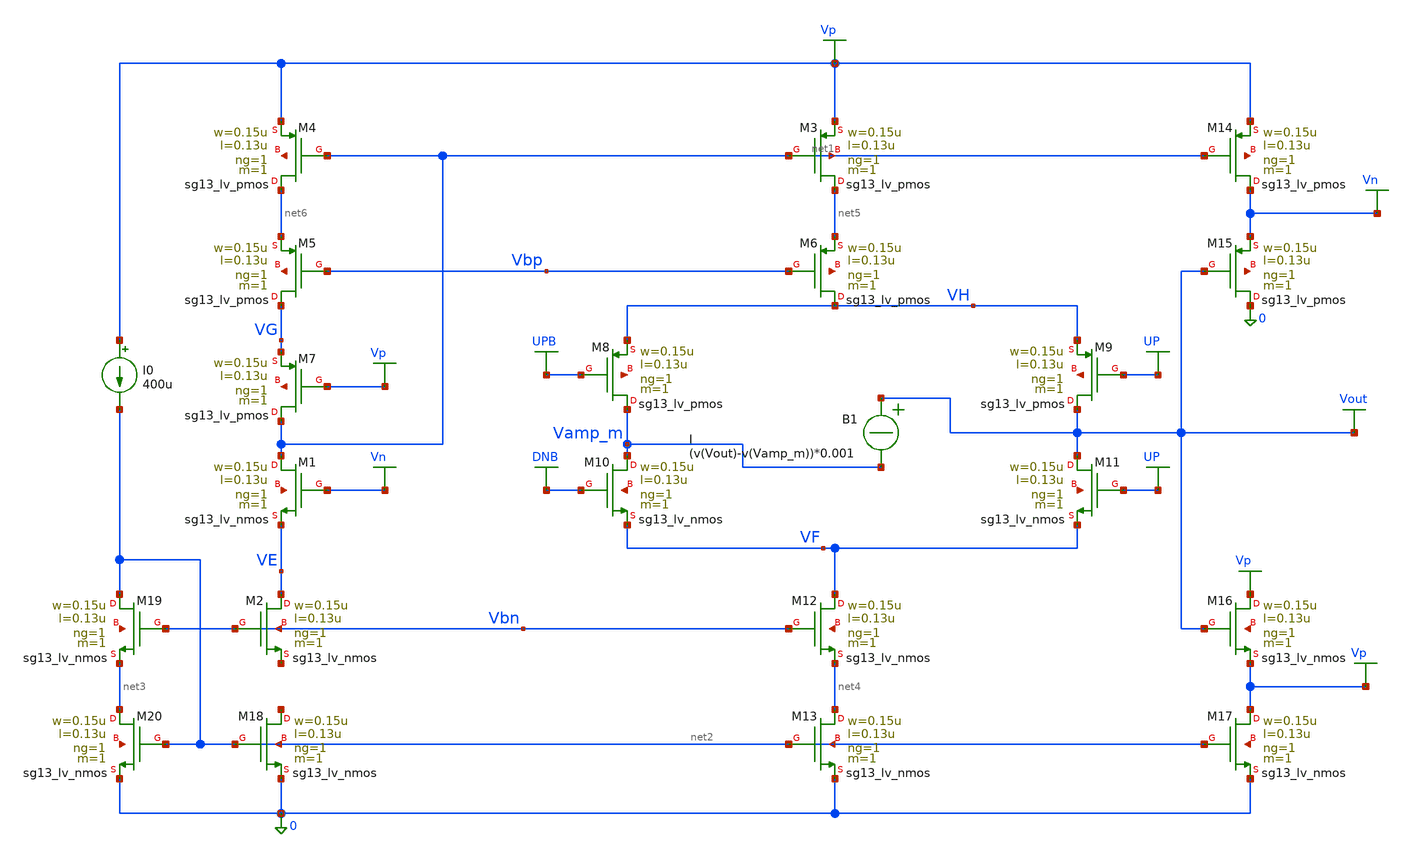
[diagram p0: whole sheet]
** sch_path: charge_pump/cp_v1.sch
**.subckt cp_v1
XM1 net1 Vn VE net7 sg13_lv_nmos w=0.15u l=0.13u ng=1 m=1 mm_ok=1
XM3 net5 net1 Vp net1 sg13_lv_pmos w=0.15u l=0.13u ng=1 m=1 mm_ok=1
XM4 net6 net1 Vp net8 sg13_lv_pmos w=0.15u l=0.13u ng=1 m=1 mm_ok=1
XM5 VG Vbp net6 net9 sg13_lv_pmos w=0.15u l=0.13u ng=1 m=1 mm_ok=1
XM6 VH Vbp net5 net10 sg13_lv_pmos w=0.15u l=0.13u ng=1 m=1 mm_ok=1
XM7 net1 Vp VG net11 sg13_lv_pmos w=0.15u l=0.13u ng=1 m=1 mm_ok=1
XM8 Vamp_m UPB VH net12 sg13_lv_pmos w=0.15u l=0.13u ng=1 m=1 mm_ok=1
XM9 Vout UP VH net13 sg13_lv_pmos w=0.15u l=0.13u ng=1 m=1 mm_ok=1
XM10 Vamp_m DNB VF net14 sg13_lv_nmos w=0.15u l=0.13u ng=1 m=1 mm_ok=1
XM11 Vout UP VF net15 sg13_lv_nmos w=0.15u l=0.13u ng=1 m=1 mm_ok=1
XM12 VF Vbn net4 net16 sg13_lv_nmos w=0.15u l=0.13u ng=1 m=1 mm_ok=1
XM13 net4 net2 0 net2 sg13_lv_nmos w=0.15u l=0.13u ng=1 m=1 mm_ok=1
XM14 Vn net1 Vp net17 sg13_lv_pmos w=0.15u l=0.13u ng=1 m=1 mm_ok=1
XM15 0 Vout Vn net18 sg13_lv_pmos w=0.15u l=0.13u ng=1 m=1 mm_ok=1
XM16 Vp Vout Vp net19 sg13_lv_nmos w=0.15u l=0.13u ng=1 m=1 mm_ok=1
XM17 Vp net2 0 net20 sg13_lv_nmos w=0.15u l=0.13u ng=1 m=1 mm_ok=1
XM2 VE Vbn net21 Vbn sg13_lv_nmos w=0.15u l=0.13u ng=1 m=1 mm_ok=1
XM18 net22 net2 0 net2 sg13_lv_nmos w=0.15u l=0.13u ng=1 m=1 mm_ok=1
XM19 net2 Vbn net3 net23 sg13_lv_nmos w=0.15u l=0.13u ng=1 m=1 mm_ok=1
XM20 net3 net2 0 net24 sg13_lv_nmos w=0.15u l=0.13u ng=1 m=1 mm_ok=1
I0 Vp net2 400u
B1 Vout Vamp_m I = (v(Vout)-v(Vamp_m))*0.001
**.ends
.GLOBAL Vp
.GLOBAL Vn
.GLOBAL UP
.GLOBAL DNB
.GLOBAL UPB
.GLOBAL Vout
.end
